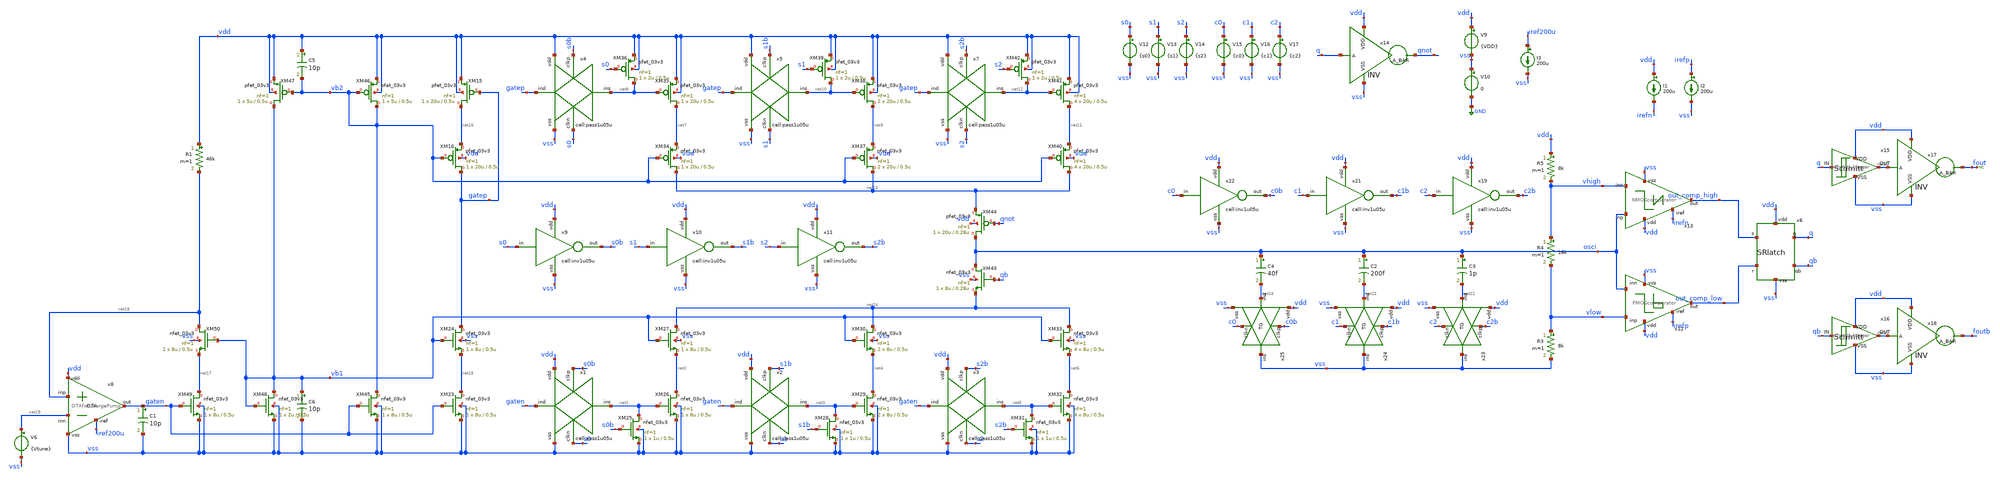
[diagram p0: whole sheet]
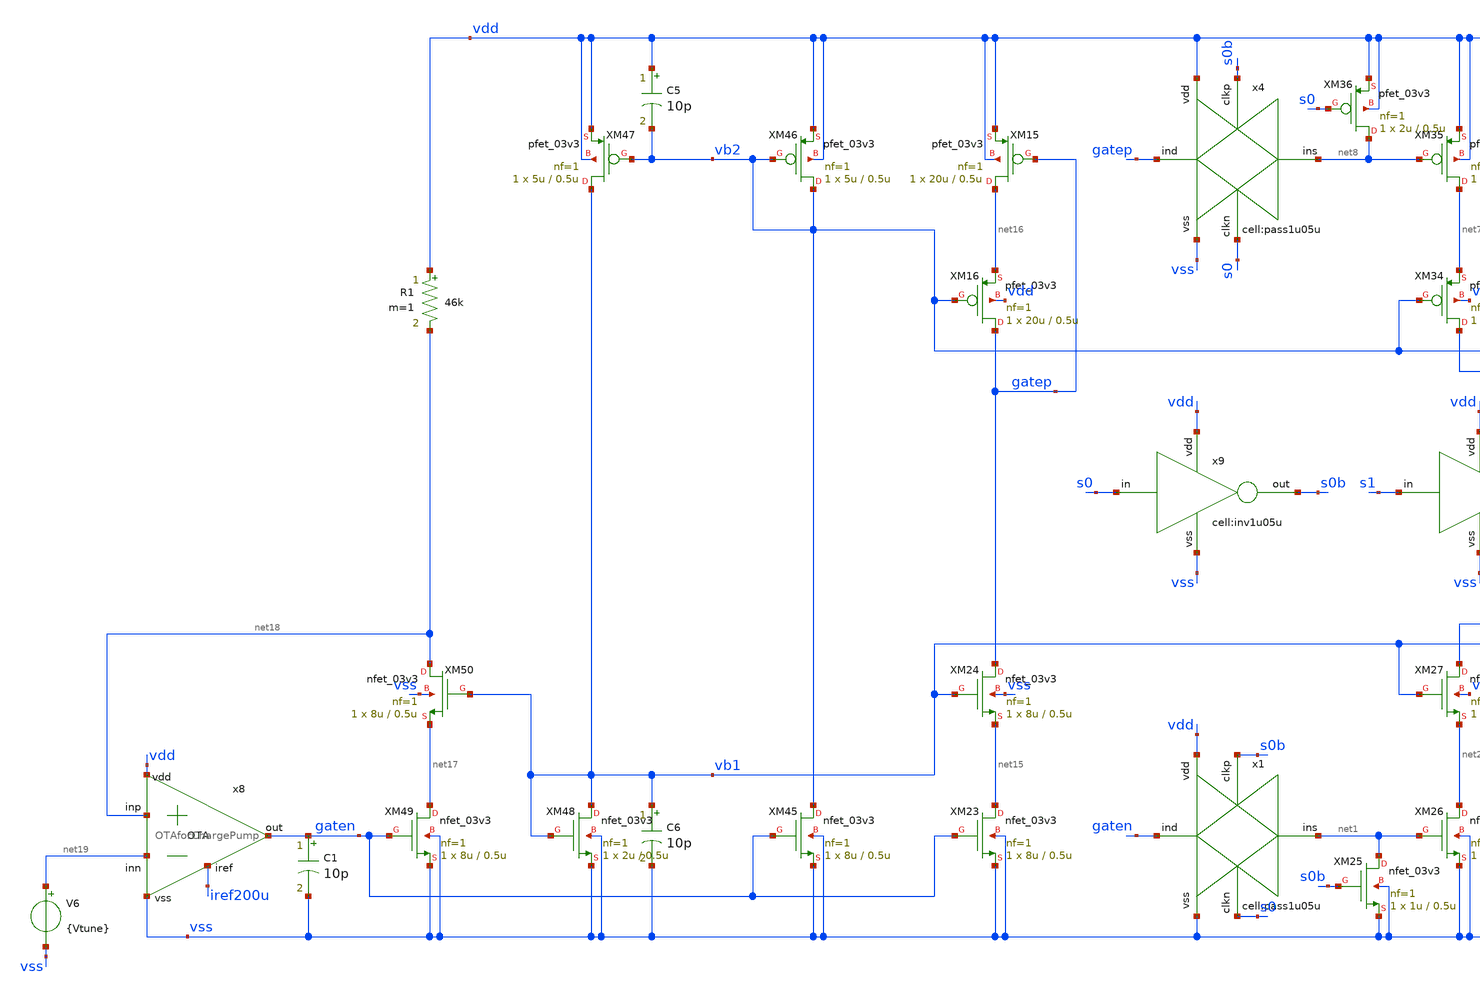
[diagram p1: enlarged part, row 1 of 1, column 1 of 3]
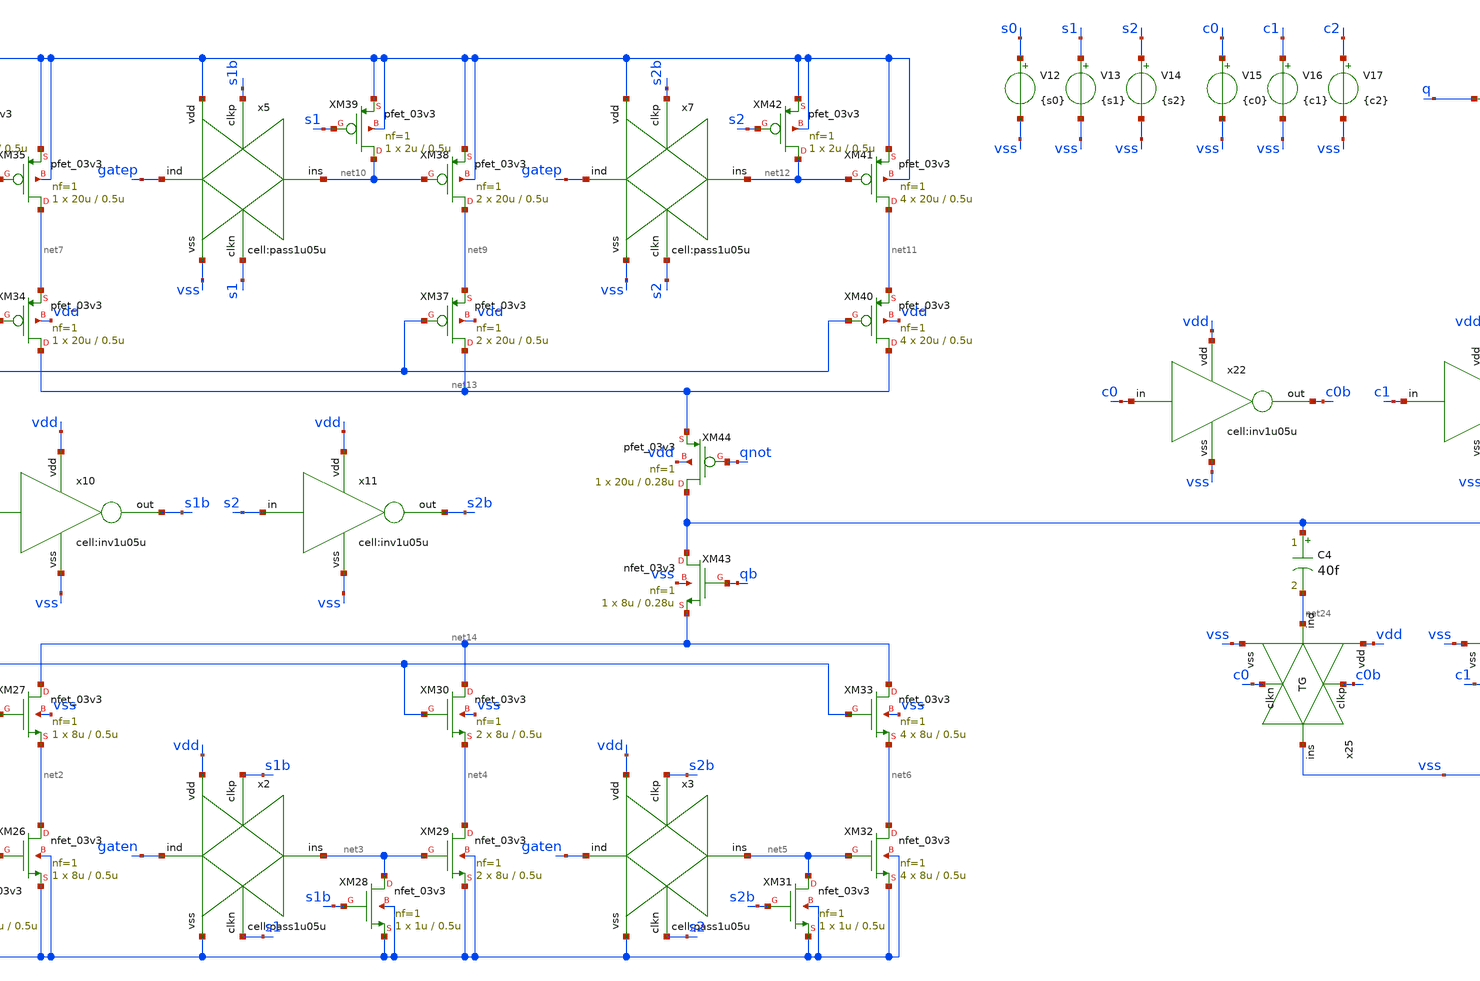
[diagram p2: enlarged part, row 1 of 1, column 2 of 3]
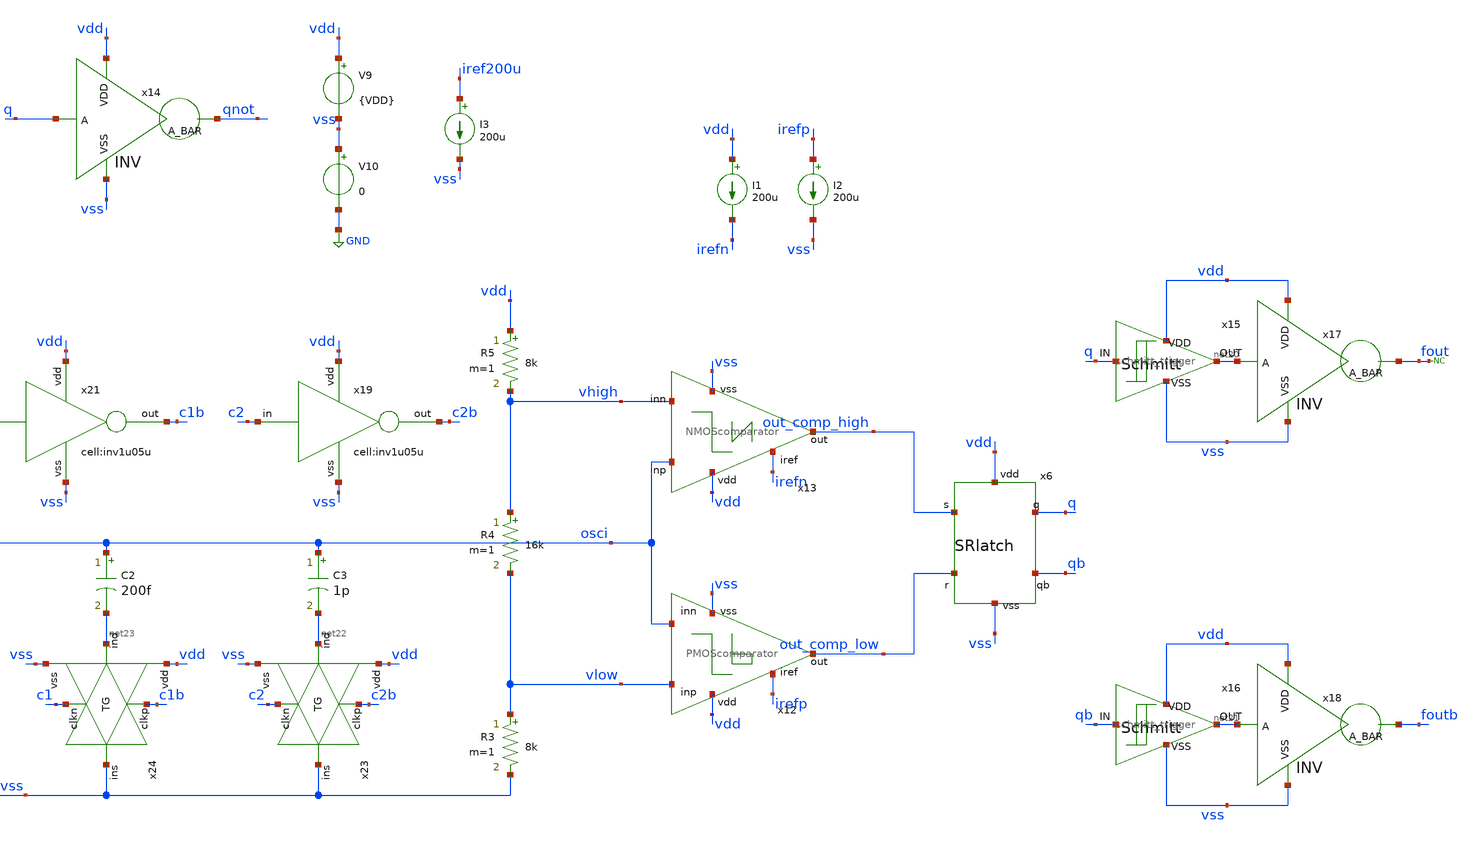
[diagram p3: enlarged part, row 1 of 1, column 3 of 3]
** sch_path: designs/libs/qw_tb_analog/PCP0817_tb/PCP0817_tb.sch
**.subckt PCP0817_tb
x1 gaten vss s0 net1 s0b vdd pass1u05u
XM25 net1 s0b vss vss nfet_03v3 L=0.5u W=1u nf=1 ad='int((nf+1)/2) * W/nf * 0.18u' as='int((nf+2)/2) * W/nf * 0.18u'
+ pd='2*int((nf+1)/2) * (W/nf + 0.18u)' ps='2*int((nf+2)/2) * (W/nf + 0.18u)' nrd='0.18u / W' nrs='0.18u / W'
+ sa=0 sb=0 sd=0 m=1
XM26 net2 net1 vss vss nfet_03v3 L=0.5u W=8u nf=1 ad='int((nf+1)/2) * W/nf * 0.18u' as='int((nf+2)/2) * W/nf * 0.18u'
+ pd='2*int((nf+1)/2) * (W/nf + 0.18u)' ps='2*int((nf+2)/2) * (W/nf + 0.18u)' nrd='0.18u / W' nrs='0.18u / W'
+ sa=0 sb=0 sd=0 m=1
XM27 net14 vb1 net2 vss nfet_03v3 L=0.5u W=8u nf=1 ad='int((nf+1)/2) * W/nf * 0.18u' as='int((nf+2)/2) * W/nf * 0.18u'
+ pd='2*int((nf+1)/2) * (W/nf + 0.18u)' ps='2*int((nf+2)/2) * (W/nf + 0.18u)' nrd='0.18u / W' nrs='0.18u / W'
+ sa=0 sb=0 sd=0 m=1
x2 gaten vss s1 net3 s1b vdd pass1u05u
XM28 net3 s1b vss vss nfet_03v3 L=0.5u W=1u nf=1 ad='int((nf+1)/2) * W/nf * 0.18u' as='int((nf+2)/2) * W/nf * 0.18u'
+ pd='2*int((nf+1)/2) * (W/nf + 0.18u)' ps='2*int((nf+2)/2) * (W/nf + 0.18u)' nrd='0.18u / W' nrs='0.18u / W'
+ sa=0 sb=0 sd=0 m=1
XM29 net4 net3 vss vss nfet_03v3 L=0.5u W=8u nf=1 ad='int((nf+1)/2) * W/nf * 0.18u' as='int((nf+2)/2) * W/nf * 0.18u'
+ pd='2*int((nf+1)/2) * (W/nf + 0.18u)' ps='2*int((nf+2)/2) * (W/nf + 0.18u)' nrd='0.18u / W' nrs='0.18u / W'
+ sa=0 sb=0 sd=0 m=2
XM30 net14 vb1 net4 vss nfet_03v3 L=0.5u W=8u nf=1 ad='int((nf+1)/2) * W/nf * 0.18u' as='int((nf+2)/2) * W/nf * 0.18u'
+ pd='2*int((nf+1)/2) * (W/nf + 0.18u)' ps='2*int((nf+2)/2) * (W/nf + 0.18u)' nrd='0.18u / W' nrs='0.18u / W'
+ sa=0 sb=0 sd=0 m=2
x3 gaten vss s2 net5 s2b vdd pass1u05u
XM31 net5 s2b vss vss nfet_03v3 L=0.5u W=1u nf=1 ad='int((nf+1)/2) * W/nf * 0.18u' as='int((nf+2)/2) * W/nf * 0.18u'
+ pd='2*int((nf+1)/2) * (W/nf + 0.18u)' ps='2*int((nf+2)/2) * (W/nf + 0.18u)' nrd='0.18u / W' nrs='0.18u / W'
+ sa=0 sb=0 sd=0 m=1
XM32 net6 net5 vss vss nfet_03v3 L=0.5u W=8u nf=1 ad='int((nf+1)/2) * W/nf * 0.18u' as='int((nf+2)/2) * W/nf * 0.18u'
+ pd='2*int((nf+1)/2) * (W/nf + 0.18u)' ps='2*int((nf+2)/2) * (W/nf + 0.18u)' nrd='0.18u / W' nrs='0.18u / W'
+ sa=0 sb=0 sd=0 m=4
XM33 net14 vb1 net6 vss nfet_03v3 L=0.5u W=8u nf=1 ad='int((nf+1)/2) * W/nf * 0.18u' as='int((nf+2)/2) * W/nf * 0.18u'
+ pd='2*int((nf+1)/2) * (W/nf + 0.18u)' ps='2*int((nf+2)/2) * (W/nf + 0.18u)' nrd='0.18u / W' nrs='0.18u / W'
+ sa=0 sb=0 sd=0 m=4
XM34 net13 vb2 net7 vdd pfet_03v3 L=0.5u W=20u nf=1 ad='int((nf+1)/2) * W/nf * 0.18u' as='int((nf+2)/2) * W/nf * 0.18u'
+ pd='2*int((nf+1)/2) * (W/nf + 0.18u)' ps='2*int((nf+2)/2) * (W/nf + 0.18u)' nrd='0.18u / W' nrs='0.18u / W'
+ sa=0 sb=0 sd=0 m=1
XM35 net7 net8 vdd vdd pfet_03v3 L=0.5u W=20u nf=1 ad='int((nf+1)/2) * W/nf * 0.18u' as='int((nf+2)/2) * W/nf * 0.18u'
+ pd='2*int((nf+1)/2) * (W/nf + 0.18u)' ps='2*int((nf+2)/2) * (W/nf + 0.18u)' nrd='0.18u / W' nrs='0.18u / W'
+ sa=0 sb=0 sd=0 m=1
x4 gatep vss s0 net8 s0b vdd pass1u05u
XM36 net8 s0 vdd vdd pfet_03v3 L=0.5u W=2u nf=1 ad='int((nf+1)/2) * W/nf * 0.18u' as='int((nf+2)/2) * W/nf * 0.18u'
+ pd='2*int((nf+1)/2) * (W/nf + 0.18u)' ps='2*int((nf+2)/2) * (W/nf + 0.18u)' nrd='0.18u / W' nrs='0.18u / W'
+ sa=0 sb=0 sd=0 m=1
XM37 net13 vb2 net9 vdd pfet_03v3 L=0.5u W=20u nf=1 ad='int((nf+1)/2) * W/nf * 0.18u' as='int((nf+2)/2) * W/nf * 0.18u'
+ pd='2*int((nf+1)/2) * (W/nf + 0.18u)' ps='2*int((nf+2)/2) * (W/nf + 0.18u)' nrd='0.18u / W' nrs='0.18u / W'
+ sa=0 sb=0 sd=0 m=2
XM38 net9 net10 vdd vdd pfet_03v3 L=0.5u W=20u nf=1 ad='int((nf+1)/2) * W/nf * 0.18u' as='int((nf+2)/2) * W/nf * 0.18u'
+ pd='2*int((nf+1)/2) * (W/nf + 0.18u)' ps='2*int((nf+2)/2) * (W/nf + 0.18u)' nrd='0.18u / W' nrs='0.18u / W'
+ sa=0 sb=0 sd=0 m=2
x5 gatep vss s1 net10 s1b vdd pass1u05u
XM39 net10 s1 vdd vdd pfet_03v3 L=0.5u W=2u nf=1 ad='int((nf+1)/2) * W/nf * 0.18u' as='int((nf+2)/2) * W/nf * 0.18u'
+ pd='2*int((nf+1)/2) * (W/nf + 0.18u)' ps='2*int((nf+2)/2) * (W/nf + 0.18u)' nrd='0.18u / W' nrs='0.18u / W'
+ sa=0 sb=0 sd=0 m=1
XM40 net13 vb2 net11 vdd pfet_03v3 L=0.5u W=20u nf=1 ad='int((nf+1)/2) * W/nf * 0.18u' as='int((nf+2)/2) * W/nf * 0.18u'
+ pd='2*int((nf+1)/2) * (W/nf + 0.18u)' ps='2*int((nf+2)/2) * (W/nf + 0.18u)' nrd='0.18u / W' nrs='0.18u / W'
+ sa=0 sb=0 sd=0 m=4
XM41 net11 net12 vdd vdd pfet_03v3 L=0.5u W=20u nf=1 ad='int((nf+1)/2) * W/nf * 0.18u' as='int((nf+2)/2) * W/nf * 0.18u'
+ pd='2*int((nf+1)/2) * (W/nf + 0.18u)' ps='2*int((nf+2)/2) * (W/nf + 0.18u)' nrd='0.18u / W' nrs='0.18u / W'
+ sa=0 sb=0 sd=0 m=4
x7 gatep vss s2 net12 s2b vdd pass1u05u
XM42 net12 s2 vdd vdd pfet_03v3 L=0.5u W=2u nf=1 ad='int((nf+1)/2) * W/nf * 0.18u' as='int((nf+2)/2) * W/nf * 0.18u'
+ pd='2*int((nf+1)/2) * (W/nf + 0.18u)' ps='2*int((nf+2)/2) * (W/nf + 0.18u)' nrd='0.18u / W' nrs='0.18u / W'
+ sa=0 sb=0 sd=0 m=1
XM43 osci qb net14 vss nfet_03v3 L=0.28u W=8u nf=1 ad='int((nf+1)/2) * W/nf * 0.18u' as='int((nf+2)/2) * W/nf * 0.18u'
+ pd='2*int((nf+1)/2) * (W/nf + 0.18u)' ps='2*int((nf+2)/2) * (W/nf + 0.18u)' nrd='0.18u / W' nrs='0.18u / W'
+ sa=0 sb=0 sd=0 m=1
XM44 osci qnot net13 vdd pfet_03v3 L=0.28u W=20u nf=1 ad='int((nf+1)/2) * W/nf * 0.18u' as='int((nf+2)/2) * W/nf * 0.18u'
+ pd='2*int((nf+1)/2) * (W/nf + 0.18u)' ps='2*int((nf+2)/2) * (W/nf + 0.18u)' nrd='0.18u / W' nrs='0.18u / W'
+ sa=0 sb=0 sd=0 m=1
XM15 net16 gatep vdd vdd pfet_03v3 L=0.5u W=20u nf=1 ad='int((nf+1)/2) * W/nf * 0.18u' as='int((nf+2)/2) * W/nf * 0.18u'
+ pd='2*int((nf+1)/2) * (W/nf + 0.18u)' ps='2*int((nf+2)/2) * (W/nf + 0.18u)' nrd='0.18u / W' nrs='0.18u / W'
+ sa=0 sb=0 sd=0 m=1
XM16 gatep vb2 net16 vdd pfet_03v3 L=0.5u W=20u nf=1 ad='int((nf+1)/2) * W/nf * 0.18u' as='int((nf+2)/2) * W/nf * 0.18u'
+ pd='2*int((nf+1)/2) * (W/nf + 0.18u)' ps='2*int((nf+2)/2) * (W/nf + 0.18u)' nrd='0.18u / W' nrs='0.18u / W'
+ sa=0 sb=0 sd=0 m=1
XM23 net15 gaten vss vss nfet_03v3 L=0.5u W=8u nf=1 ad='int((nf+1)/2) * W/nf * 0.18u' as='int((nf+2)/2) * W/nf * 0.18u'
+ pd='2*int((nf+1)/2) * (W/nf + 0.18u)' ps='2*int((nf+2)/2) * (W/nf + 0.18u)' nrd='0.18u / W' nrs='0.18u / W'
+ sa=0 sb=0 sd=0 m=1
XM24 gatep vb1 net15 vss nfet_03v3 L=0.5u W=8u nf=1 ad='int((nf+1)/2) * W/nf * 0.18u' as='int((nf+2)/2) * W/nf * 0.18u'
+ pd='2*int((nf+1)/2) * (W/nf + 0.18u)' ps='2*int((nf+2)/2) * (W/nf + 0.18u)' nrd='0.18u / W' nrs='0.18u / W'
+ sa=0 sb=0 sd=0 m=1
XM45 vb2 gaten vss vss nfet_03v3 L=0.5u W=8u nf=1 ad='int((nf+1)/2) * W/nf * 0.18u' as='int((nf+2)/2) * W/nf * 0.18u'
+ pd='2*int((nf+1)/2) * (W/nf + 0.18u)' ps='2*int((nf+2)/2) * (W/nf + 0.18u)' nrd='0.18u / W' nrs='0.18u / W'
+ sa=0 sb=0 sd=0 m=1
XM46 vb2 vb2 vdd vdd pfet_03v3 L=0.5u W=5u nf=1 ad='int((nf+1)/2) * W/nf * 0.18u' as='int((nf+2)/2) * W/nf * 0.18u'
+ pd='2*int((nf+1)/2) * (W/nf + 0.18u)' ps='2*int((nf+2)/2) * (W/nf + 0.18u)' nrd='0.18u / W' nrs='0.18u / W'
+ sa=0 sb=0 sd=0 m=1
XM47 vb1 vb2 vdd vdd pfet_03v3 L=0.5u W=5u nf=1 ad='int((nf+1)/2) * W/nf * 0.18u' as='int((nf+2)/2) * W/nf * 0.18u'
+ pd='2*int((nf+1)/2) * (W/nf + 0.18u)' ps='2*int((nf+2)/2) * (W/nf + 0.18u)' nrd='0.18u / W' nrs='0.18u / W'
+ sa=0 sb=0 sd=0 m=1
XM48 vb1 vb1 vss vss nfet_03v3 L=0.5u W=2u nf=1 ad='int((nf+1)/2) * W/nf * 0.18u' as='int((nf+2)/2) * W/nf * 0.18u'
+ pd='2*int((nf+1)/2) * (W/nf + 0.18u)' ps='2*int((nf+2)/2) * (W/nf + 0.18u)' nrd='0.18u / W' nrs='0.18u / W'
+ sa=0 sb=0 sd=0 m=1
XM49 net17 gaten vss vss nfet_03v3 L=0.5u W=8u nf=1 ad='int((nf+1)/2) * W/nf * 0.18u' as='int((nf+2)/2) * W/nf * 0.18u'
+ pd='2*int((nf+1)/2) * (W/nf + 0.18u)' ps='2*int((nf+2)/2) * (W/nf + 0.18u)' nrd='0.18u / W' nrs='0.18u / W'
+ sa=0 sb=0 sd=0 m=1
XM50 net18 vb1 net17 vss nfet_03v3 L=0.5u W=8u nf=1 ad='int((nf+1)/2) * W/nf * 0.18u' as='int((nf+2)/2) * W/nf * 0.18u'
+ pd='2*int((nf+1)/2) * (W/nf + 0.18u)' ps='2*int((nf+2)/2) * (W/nf + 0.18u)' nrd='0.18u / W' nrs='0.18u / W'
+ sa=0 sb=0 sd=0 m=1
x8 vdd iref200u net18 net19 gaten vss OTAforChargePump
R1 vdd net18 46k m=1
C1 gaten vss 10p m=1
C5 vdd vb2 10p m=1
x9 s0 vdd s0b vss inv1u05u
C6 vb1 vss 10p m=1
x10 s1 vdd s1b vss inv1u05u
x11 s2 vdd s2b vss inv1u05u
V6 net19 vss {Vtune}
V9 vdd vss {VDD}
V10 vss GND 0
I1 vdd irefn 200u
I2 irefp vss 200u
R3 vlow vss 8k m=1
R4 vhigh vlow 16k m=1
R5 vdd vhigh 8k m=1
x6 vdd out_comp_high q qb out_comp_low vss SRlatch
x12 vdd irefp vlow out_comp_low osci vss PMOScomparator
x13 vdd osci out_comp_high vhigh irefn vss NMOScomparator
x14 vdd q qnot vss INV
x15 q net20 vdd vss schmitt_trigger
x16 qb net21 vdd vss schmitt_trigger
x17 vdd net20 fout vss INV
x18 vdd net21 foutb vss INV
I3 iref200u vss 200u
* noconn fout
V12 s0 vss {s0}
V13 s1 vss {s1}
V14 s2 vss {s2}
V15 c0 vss {c0}
V16 c1 vss {c1}
V17 c2 vss {c2}
C3 osci net22 1p m=1
x19 c2 vdd c2b vss inv1u05u
C2 osci net23 200f m=1
C4 osci net24 40f m=1
x21 c1 vdd c1b vss inv1u05u
x22 c0 vdd c0b vss inv1u05u
x23 vdd c2b net22 vss vss c2 TG
x24 vdd c1b net23 vss vss c1 TG
x25 vdd c0b net24 vss vss c0 TG
**** begin user architecture code



.param VDD = 3.3
.param Vtune = 1
.param s0 = 3.3 s1 = 0 s2 = 0 c0 = 0 c1 = 0 c2 = 3.3
.param VIN=1
*V6 net3 0 {Vtune}

.control
save all

tran 10p 200n


write PCP0817_tb.raw
.endc



.include $::180MCU_MODELS/design.ngspice
.lib $::180MCU_MODELS/sm141064.ngspice typical
.lib $::180MCU_MODELS/sm141064.ngspice cap_mim
.lib $::180MCU_MODELS/sm141064.ngspice res_typical
.lib $::180MCU_MODELS/sm141064.ngspice moscap_typical
.lib $::180MCU_MODELS/sm141064.ngspice mimcap_typical
* .lib $::180MCU_MODELS/sm141064.ngspice res_statistical

**** end user architecture code
**.ends
.GLOBAL GND
.end
